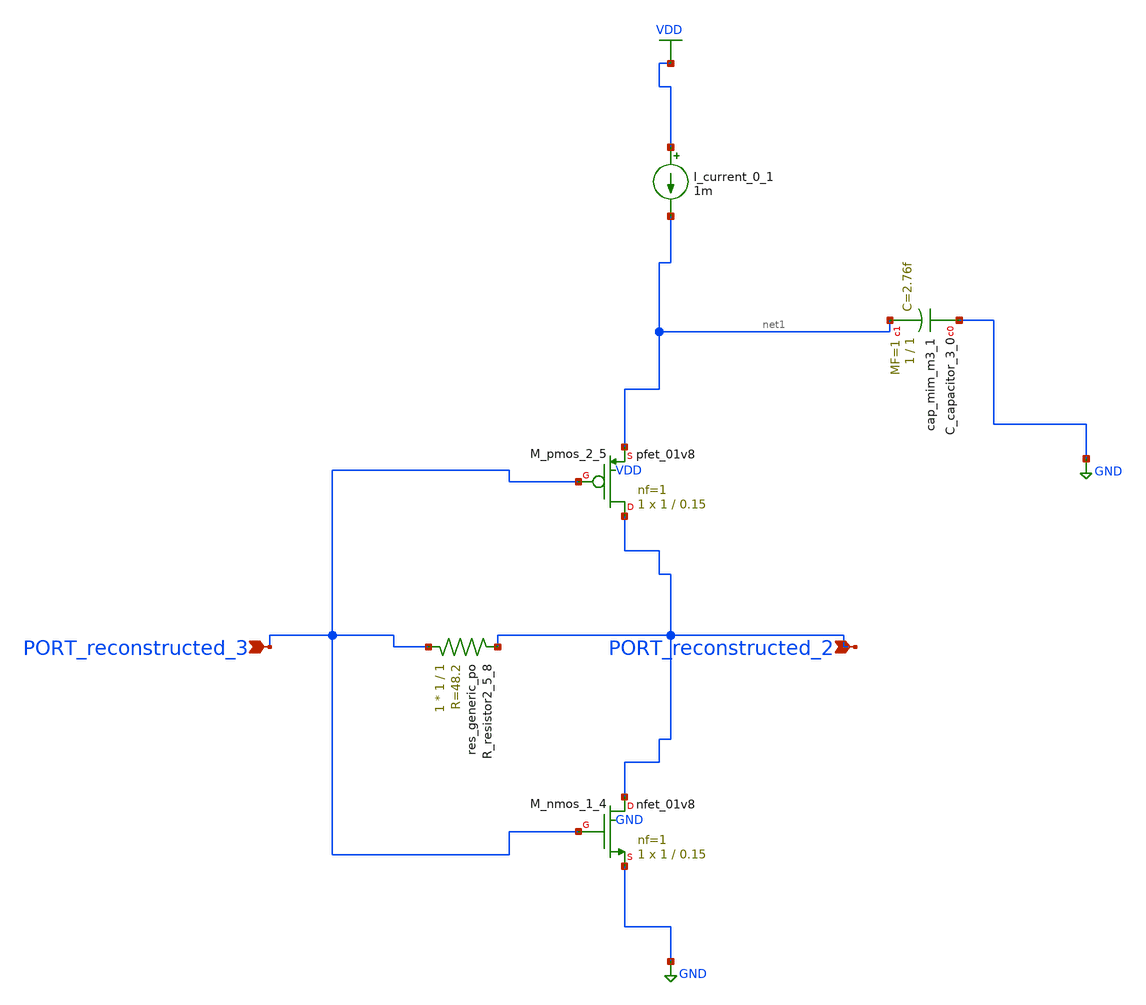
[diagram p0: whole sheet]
** sch_path: schematics/AMSNet/310.sch
**.subckt 310 PORT_reconstructed_2 PORT_reconstructed_3
*.ipin PORT_reconstructed_2
*.ipin PORT_reconstructed_3
XC_capacitor_3_0 GND net1 sky130_fd_pr__cap_mim_m3_1 W=1 L=1 MF=1 m=1
I_current_0_1 VDD net1 1m
XM_nmos_1_4 PORT_reconstructed_2 PORT_reconstructed_3 GND GND sky130_fd_pr__nfet_01v8 L=0.15 W=1 nf=1
+ ad='int((1 + 1)/2) * 1 / 1 * 0.29' as='int((1 + 2)/2) * 1 / 1 * 0.29' pd='2*int((1 + 1)/2) * (1 / 1 + 0.29)'
+ ps='2*int((1 + 2)/2) * (1 / 1 + 0.29)' nrd='0.29 / 1 ' nrs='0.29 / 1 ' sa=0 sb=0 sd=0 mult=1 m=1
XM_pmos_2_5 PORT_reconstructed_2 PORT_reconstructed_3 net1 VDD sky130_fd_pr__pfet_01v8 L=0.15 W=1 nf=1
+ ad='int((1 + 1)/2) * 1 / 1 * 0.29' as='int((1 + 2)/2) * 1 / 1 * 0.29' pd='2*int((1 + 1)/2) * (1 / 1 + 0.29)'
+ ps='2*int((1 + 2)/2) * (1 / 1 + 0.29)' nrd='0.29 / 1 ' nrs='0.29 / 1 ' sa=0 sb=0 sd=0 mult=1 m=1
XR_resistor2_5_8 PORT_reconstructed_3 PORT_reconstructed_2 sky130_fd_pr__res_generic_po W=1 L=1 m=1
**.ends
.GLOBAL GND
.GLOBAL VDD
.end
